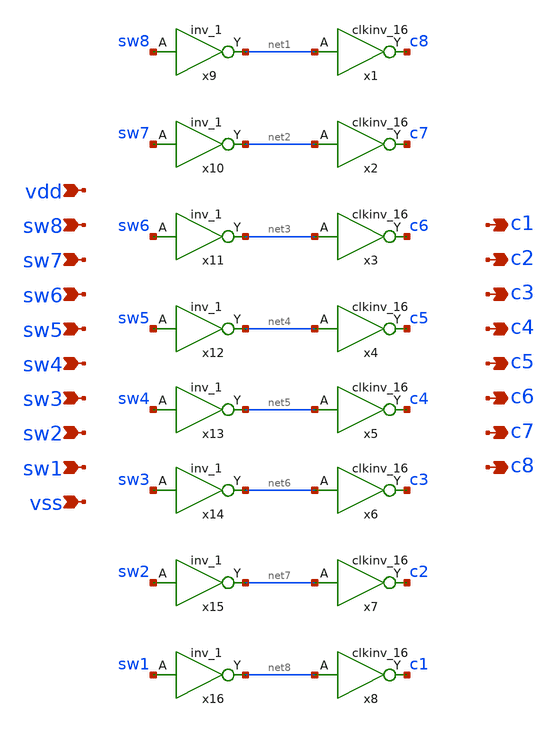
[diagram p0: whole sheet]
** sch_path: xschem/dac_sw_8b.sch
**.subckt dac_sw_8b vdd sw8 sw7 sw6 sw5 sw4 sw3 sw2 sw1 vss c8 c7 c6 c5 c4 c3 c2 c1
*.ipin vdd
*.ipin sw8
*.ipin sw7
*.ipin sw6
*.ipin sw5
*.ipin sw4
*.ipin sw3
*.ipin sw2
*.ipin sw1
*.ipin vss
*.opin c8
*.opin c7
*.opin c6
*.opin c5
*.opin c4
*.opin c3
*.opin c2
*.opin c1
x1 net1 vss vss vdd vdd c8 sky130_fd_sc_hd__clkinv_16
x2 net2 vss vss vdd vdd c7 sky130_fd_sc_hd__clkinv_16
x3 net3 vss vss vdd vdd c6 sky130_fd_sc_hd__clkinv_16
x4 net4 vss vss vdd vdd c5 sky130_fd_sc_hd__clkinv_16
x5 net5 vss vss vdd vdd c4 sky130_fd_sc_hd__clkinv_16
x6 net6 vss vss vdd vdd c3 sky130_fd_sc_hd__clkinv_16
x7 net7 vss vss vdd vdd c2 sky130_fd_sc_hd__clkinv_16
x8 net8 vss vss vdd vdd c1 sky130_fd_sc_hd__clkinv_16
x9 sw8 vss vss vdd vdd net1 sky130_fd_sc_hd__inv_1
x10 sw7 vss vss vdd vdd net2 sky130_fd_sc_hd__inv_1
x11 sw6 vss vss vdd vdd net3 sky130_fd_sc_hd__inv_1
x12 sw5 vss vss vdd vdd net4 sky130_fd_sc_hd__inv_1
x13 sw4 vss vss vdd vdd net5 sky130_fd_sc_hd__inv_1
x14 sw3 vss vss vdd vdd net6 sky130_fd_sc_hd__inv_1
x15 sw2 vss vss vdd vdd net7 sky130_fd_sc_hd__inv_1
x16 sw1 vss vss vdd vdd net8 sky130_fd_sc_hd__inv_1
**.ends
.end
